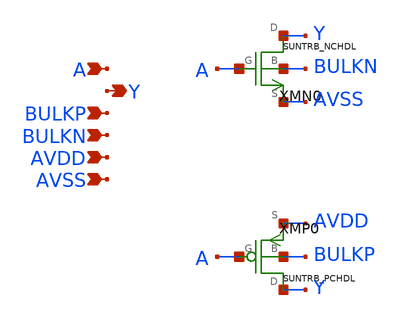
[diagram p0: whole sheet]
** sch_path: ip/sun_trb_sky130nm/design/SUN_TRB_SKY130NM/SUNTRB_IVX1_CV.sch
**.subckt SUNTRB_IVX1_CV A Y BULKP BULKN AVDD AVSS
*.ipin A
*.opin Y
*.ipin BULKP
*.ipin BULKN
*.ipin AVDD
*.ipin AVSS
XMN0 Y A AVSS BULKN SUNTRB_NCHDL xoffset=0 yoffset=0 angle=0
XMP0 Y A AVDD BULKP SUNTRB_PCHDL xoffset=0 yoffset=0 angle=0
**.ends
.end
